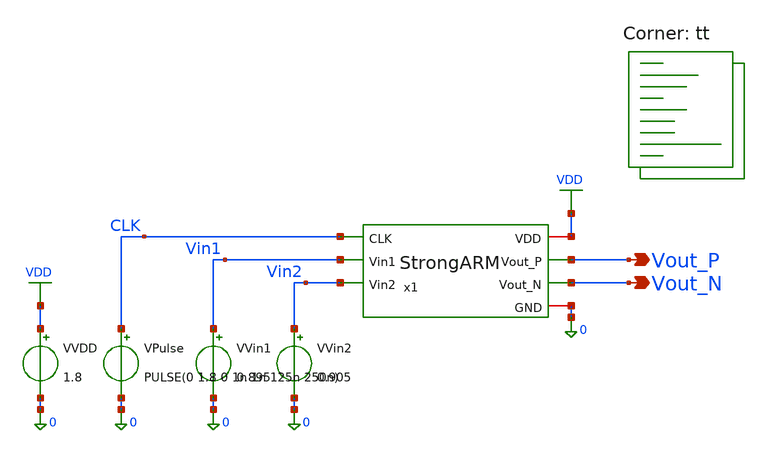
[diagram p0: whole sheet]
** sch_path: blocks/03_StrongARM/sim/tb_StrongARM_Transient.sch
**.subckt tb_StrongARM_Transient Vout_P Vout_N
*.opin Vout_P
*.opin Vout_N
x1 VDD CLK Vout_P Vout_N Vin1 Vin2 0 StrongARM
VVDD VDD 0 1.8
VVin1 Vin1 0 0.895
VVin2 Vin2 0 0.905
VPulse CLK 0 PULSE(0 1.8 0 1n 1n 125n 250n)
**** begin user architecture code


.control
save all

* =========================================
* BLOCK 3 - STRONGARM COMPARATOR
* TEST 6A: NOMINAL INPUT OFFSET SWEEP
* SKY130 / VDD = 1.8 V / CLK = 4 MHz
* Input common mode = 0.9 V
* =========================================

foreach dv 0.001 0.0005 0.0002 0.0001 0.00005 0 -0.00005 -0.0001 -0.0002 -0.0005 -0.001

  setplot const

  let vip = 0.9 + ($dv / 2)
  let vin = 0.9 - ($dv / 2)

  alter VVIN1 $&vip
  alter VVIN2 $&vin

  echo
  echo ======================================
  echo TEST 6A - NOMINAL OFFSET SWEEP
  echo DIFFERENTIAL INPUT = $dv V
  echo ======================================

  tran 0.1n 1u

  * Evaluate second clock cycle
  meas tran vp_eval FIND v(vout_p) AT=362.5n
  meas tran vn_eval FIND v(vout_n) AT=362.5n

  * Check earlier evaluation point
  meas tran vp_early FIND v(vout_p) AT=262.5n
  meas tran vn_early FIND v(vout_n) AT=262.5n

  * Check reset
  meas tran vp_reset FIND v(vout_p) AT=437.5n
  meas tran vn_reset FIND v(vout_n) AT=437.5n

  echo ======================================
  echo END OF OFFSET POINT
  echo ======================================

  reset

end

echo
echo ALL 11 OFFSET POINTS COMPLETED
echo

.endc

.lib $::SKYWATER_MODELS/sky130.lib.spice tt
**** end user architecture code
**.ends

* expanding   symbol:  blocks/03_StrongARM/xschem/StrongARM.sym # of pins=7
** sym_path: blocks/03_StrongARM/xschem/StrongARM.sym
** sch_path: blocks/03_StrongARM/xschem/StrongARM.sch
.subckt StrongARM VDD CLK Vout_P Vout_N Vin1 Vin2 GND
*.iopin VDD
*.iopin GND
*.ipin Vin1
*.ipin Vin2
*.ipin CLK
*.opin Vout_P
*.opin Vout_N
XS1 P CLK VDD VDD sky130_fd_pr__pfet_01v8 L=0.15 W=1.5 nf=1 ad='int((1 + 1)/2) * 1.5 / 1 * 0.29' as='int((1 + 2)/2) * 1.5 / 1 * 0.29'
+ pd='2*int((1 + 1)/2) * (1.5 / 1 + 0.29)' ps='2*int((1 + 2)/2) * (1.5 / 1 + 0.29)' nrd='0.29 / 1.5 ' nrs='0.29 / 1.5 '
+ sa=0 sb=0 sd=0 mult=1 m=1
XS3 Vout_P CLK VDD VDD sky130_fd_pr__pfet_01v8 L=0.15 W=1.5 nf=1 ad='int((1 + 1)/2) * 1.5 / 1 * 0.29'
+ as='int((1 + 2)/2) * 1.5 / 1 * 0.29' pd='2*int((1 + 1)/2) * (1.5 / 1 + 0.29)' ps='2*int((1 + 2)/2) * (1.5 / 1 + 0.29)'
+ nrd='0.29 / 1.5 ' nrs='0.29 / 1.5 ' sa=0 sb=0 sd=0 mult=1 m=1
XM5 Vout_P Vout_N VDD VDD sky130_fd_pr__pfet_01v8 L=0.3 W=5 nf=1 ad='int((1 + 1)/2) * 5 / 1 * 0.29' as='int((1 + 2)/2) * 5 / 1 * 0.29'
+ pd='2*int((1 + 1)/2) * (5 / 1 + 0.29)' ps='2*int((1 + 2)/2) * (5 / 1 + 0.29)' nrd='0.29 / 5 ' nrs='0.29 / 5 '
+ sa=0 sb=0 sd=0 mult=1 m=1
XM6 Vout_N Vout_P VDD VDD sky130_fd_pr__pfet_01v8 L=0.3 W=5 nf=1 ad='int((1 + 1)/2) * 5 / 1 * 0.29' as='int((1 + 2)/2) * 5 / 1 * 0.29'
+ pd='2*int((1 + 1)/2) * (5 / 1 + 0.29)' ps='2*int((1 + 2)/2) * (5 / 1 + 0.29)' nrd='0.29 / 5 ' nrs='0.29 / 5 '
+ sa=0 sb=0 sd=0 mult=1 m=1
XS4 Vout_N CLK VDD VDD sky130_fd_pr__pfet_01v8 L=0.15 W=1.5 nf=1 ad='int((1 + 1)/2) * 1.5 / 1 * 0.29'
+ as='int((1 + 2)/2) * 1.5 / 1 * 0.29' pd='2*int((1 + 1)/2) * (1.5 / 1 + 0.29)' ps='2*int((1 + 2)/2) * (1.5 / 1 + 0.29)'
+ nrd='0.29 / 1.5 ' nrs='0.29 / 1.5 ' sa=0 sb=0 sd=0 mult=1 m=1
XS2 Q CLK VDD VDD sky130_fd_pr__pfet_01v8 L=0.15 W=1.5 nf=1 ad='int((1 + 1)/2) * 1.5 / 1 * 0.29' as='int((1 + 2)/2) * 1.5 / 1 * 0.29'
+ pd='2*int((1 + 1)/2) * (1.5 / 1 + 0.29)' ps='2*int((1 + 2)/2) * (1.5 / 1 + 0.29)' nrd='0.29 / 1.5 ' nrs='0.29 / 1.5 '
+ sa=0 sb=0 sd=0 mult=1 m=1
XM3 Vout_P Vout_N P GND sky130_fd_pr__nfet_01v8 L=0.3 W=2 nf=1 ad='int((1 + 1)/2) * 2 / 1 * 0.29' as='int((1 + 2)/2) * 2 / 1 * 0.29'
+ pd='2*int((1 + 1)/2) * (2 / 1 + 0.29)' ps='2*int((1 + 2)/2) * (2 / 1 + 0.29)' nrd='0.29 / 2 ' nrs='0.29 / 2 '
+ sa=0 sb=0 sd=0 mult=1 m=1
XM4 Vout_N Vout_P Q GND sky130_fd_pr__nfet_01v8 L=0.3 W=2 nf=1 ad='int((1 + 1)/2) * 2 / 1 * 0.29' as='int((1 + 2)/2) * 2 / 1 * 0.29'
+ pd='2*int((1 + 1)/2) * (2 / 1 + 0.29)' ps='2*int((1 + 2)/2) * (2 / 1 + 0.29)' nrd='0.29 / 2 ' nrs='0.29 / 2 '
+ sa=0 sb=0 sd=0 mult=1 m=1
XM1 P Vin1 TAIL GND sky130_fd_pr__nfet_01v8 L=0.5 W=10 nf=1 ad='int((1 + 1)/2) * 10 / 1 * 0.29' as='int((1 + 2)/2) * 10 / 1 * 0.29'
+ pd='2*int((1 + 1)/2) * (10 / 1 + 0.29)' ps='2*int((1 + 2)/2) * (10 / 1 + 0.29)' nrd='0.29 / 10 ' nrs='0.29 / 10 '
+ sa=0 sb=0 sd=0 mult=1 m=1
XM2 Q Vin2 TAIL GND sky130_fd_pr__nfet_01v8 L=0.5 W=10 nf=1 ad='int((1 + 1)/2) * 10 / 1 * 0.29' as='int((1 + 2)/2) * 10 / 1 * 0.29'
+ pd='2*int((1 + 1)/2) * (10 / 1 + 0.29)' ps='2*int((1 + 2)/2) * (10 / 1 + 0.29)' nrd='0.29 / 10 ' nrs='0.29 / 10 '
+ sa=0 sb=0 sd=0 mult=1 m=1
XM7 TAIL CLK GND GND sky130_fd_pr__nfet_01v8 L=0.3 W=1 nf=1 ad='int((1 + 1)/2) * 1 / 1 * 0.29' as='int((1 + 2)/2) * 1 / 1 * 0.29'
+ pd='2*int((1 + 1)/2) * (1 / 1 + 0.29)' ps='2*int((1 + 2)/2) * (1 / 1 + 0.29)' nrd='0.29 / 1 ' nrs='0.29 / 1 '
+ sa=0 sb=0 sd=0 mult=1 m=1
.ends

.GLOBAL VDD
.end
